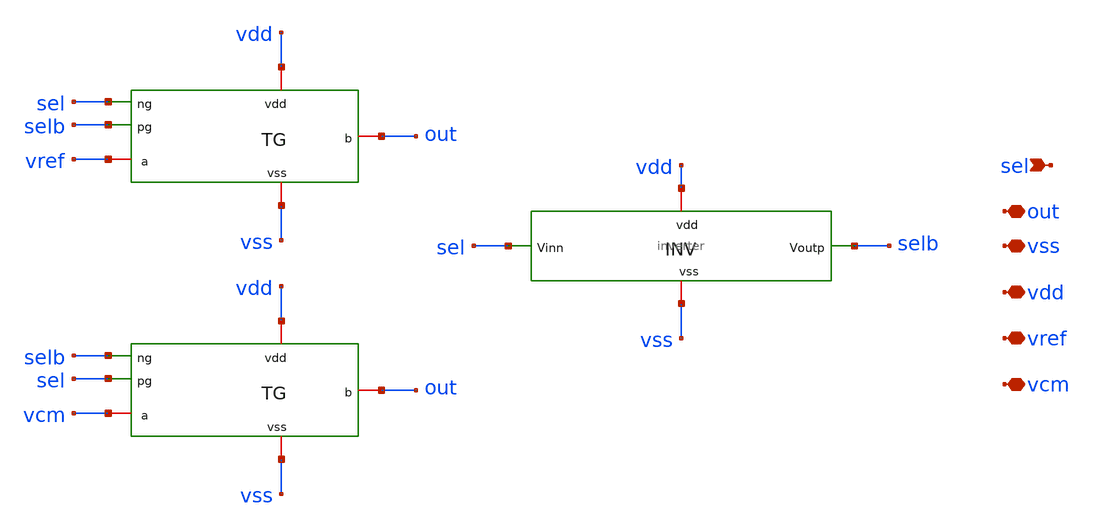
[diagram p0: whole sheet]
** sch_path: circuit_files/sar_adc_test/xschem/dac_sw_2to1_tg.sch
**.subckt dac_sw_2to1_tg sel vdd vref vcm vss out
*.ipin sel
*.iopin vdd
*.iopin vref
*.iopin vcm
*.iopin vss
*.iopin out
x1 vss sel selb vdd vref out tg
x3 vss selb sel vdd vcm out tg
x2 vdd sel selb vss inverter
**.ends

* expanding   symbol:  /home/arjun/eda/projects/SAR_ADC/circuit_files/sar_adc_test/xschem/tg.sym #
*+ of pins=6
** sym_path: circuit_files/sar_adc_test/xschem/tg.sym
** sch_path: circuit_files/sar_adc_test/xschem/tg.sch
.subckt tg vss ng pg vdd a b
*.ipin ng
*.iopin vdd
*.ipin pg
*.iopin a
*.iopin b
*.iopin vss
XM12 b ng a vss sg13_hv_nmos w=2u l=0.45u ng=1 m=1 mm_ok=1
XM16 b pg a vdd sg13_hv_pmos w=2u l=0.4u ng=1 m=2 mm_ok=1
.ends


* expanding   symbol:
*+  /home/arjun/eda/projects/SAR_ADC/circuit_files/sar_adc_test/xschem/inverter.sym # of pins=4
** sym_path: circuit_files/sar_adc_test/xschem/inverter.sym
** sch_path: circuit_files/sar_adc_test/xschem/inverter.sch
.subckt inverter vdd Vinn Voutp vss
*.iopin vdd
*.iopin vss
*.ipin Vinn
*.opin Voutp
XM12 Voutp Vinn vss vss sg13_hv_nmos w=2u l=0.45u ng=1 m=1 mm_ok=1
XM16 Voutp Vinn vdd vdd sg13_hv_pmos w=2u l=0.4u ng=1 m=2 mm_ok=1
.ends

.end
